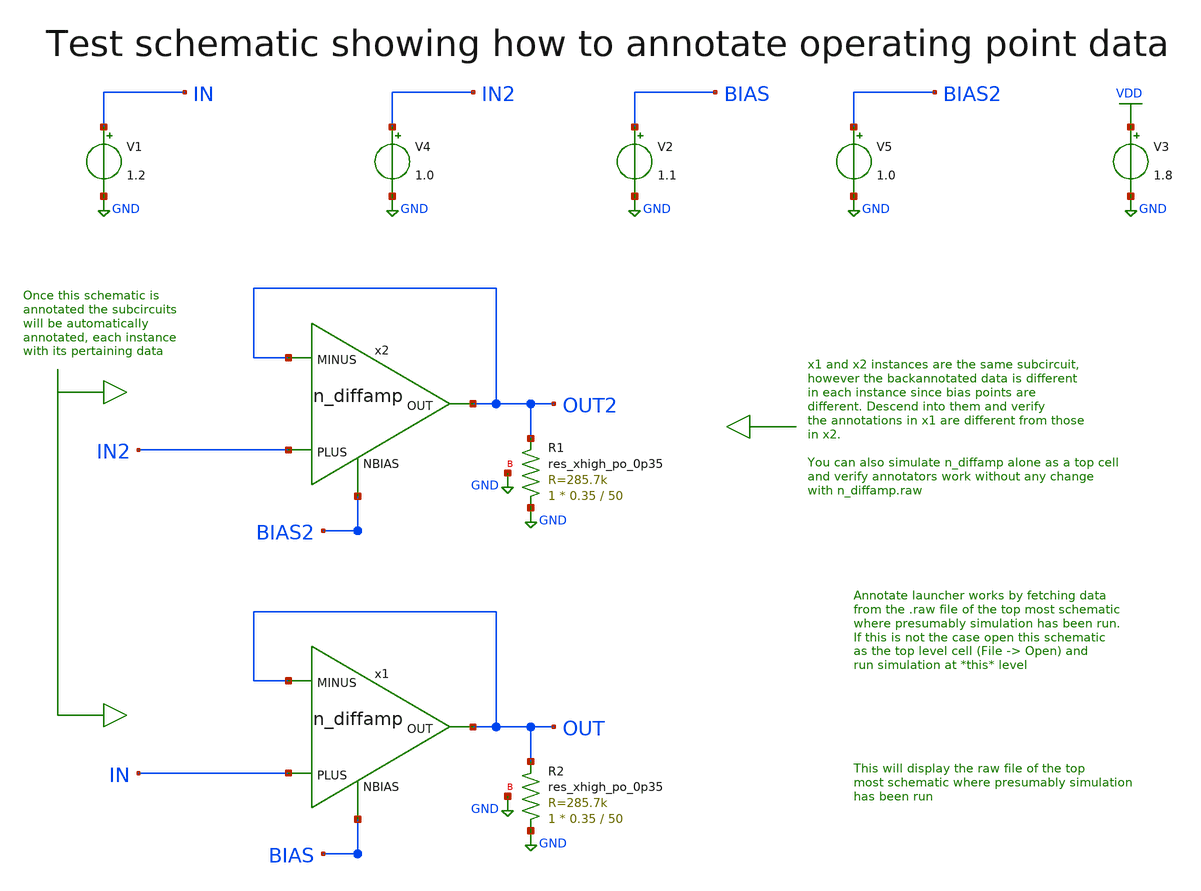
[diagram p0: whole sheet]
** sch_path: sky130_tests/test_analog.sch
* Copyright 2021 Stefan Frederik Schippers
* Licensed under the Apache License, Version 2.0 (the "License");
* you may not use this file except in compliance with the License.
* You may obtain a copy of the License at
* https://www.apache.org/licenses/LICENSE-2.0
* Unless required by applicable law or agreed to in writing, software
* distributed under the License is distributed on an "AS IS" BASIS,
* WITHOUT WARRANTIES OR CONDITIONS OF ANY KIND, either express or implied.
* See the License for the specific language governing permissions and
* limitations under the License.
**.subckt test_analog
x1 OUT OUT IN BIAS n_diffamp
x2 OUT2 OUT2 IN2 BIAS2 n_diffamp
V1 IN GND 1.2
V2 BIAS GND 1.1
V3 VDD GND 1.8
V4 IN2 GND 1.0
V5 BIAS2 GND 1.0
XR1 GND OUT2 GND sky130_fd_pr__res_xhigh_po_0p35 L=50 mult=1 m=1
XR2 GND OUT GND sky130_fd_pr__res_xhigh_po_0p35 L=50 mult=1 m=1
**** begin user architecture code

** opencircuitdesign pdks install
.lib $::SKYWATER_MODELS/sky130.lib.spice tt


**** end user architecture code
**.ends

* expanding   symbol:  sky130_tests/n_diffamp.sym # of pins=4
** sym_path: sky130_tests/n_diffamp.sym
** sch_path: sky130_tests/n_diffamp.sch
.subckt n_diffamp OUT MINUS PLUS NBIAS
*.ipin PLUS
*.ipin MINUS
*.opin OUT
*.ipin NBIAS
XM1 net1 PLUS S GND sky130_fd_pr__nfet_01v8_lvt L=0.3 W=2 nf=1 ad='int((nf+1)/2) * W/nf * 0.29' as='int((nf+2)/2) * W/nf * 0.29'
+ pd='2*int((nf+1)/2) * (W/nf + 0.29)' ps='2*int((nf+2)/2) * (W/nf + 0.29)' nrd='0.29 / W' nrs='0.29 / W'
+ sa=0 sb=0 sd=0 mult=1 m=1
XM2 OUT MINUS S GND sky130_fd_pr__nfet_01v8_lvt L=0.3 W=2 nf=1 ad='int((nf+1)/2) * W/nf * 0.29' as='int((nf+2)/2) * W/nf * 0.29'
+ pd='2*int((nf+1)/2) * (W/nf + 0.29)' ps='2*int((nf+2)/2) * (W/nf + 0.29)' nrd='0.29 / W' nrs='0.29 / W'
+ sa=0 sb=0 sd=0 mult=1 m=1
XM3 OUT net1 VDD VDD sky130_fd_pr__pfet_01v8_lvt L=0.8 W=4 nf=1 ad='int((nf+1)/2) * W/nf * 0.29' as='int((nf+2)/2) * W/nf * 0.29'
+ pd='2*int((nf+1)/2) * (W/nf + 0.29)' ps='2*int((nf+2)/2) * (W/nf + 0.29)' nrd='0.29 / W' nrs='0.29 / W'
+ sa=0 sb=0 sd=0 mult=1 m=1
XM4 net1 net1 VDD VDD sky130_fd_pr__pfet_01v8_lvt L=0.8 W=4 nf=1 ad='int((nf+1)/2) * W/nf * 0.29' as='int((nf+2)/2) * W/nf * 0.29'
+ pd='2*int((nf+1)/2) * (W/nf + 0.29)' ps='2*int((nf+2)/2) * (W/nf + 0.29)' nrd='0.29 / W' nrs='0.29 / W'
+ sa=0 sb=0 sd=0 mult=1 m=1
XM5 net2 NBIAS GND GND sky130_fd_pr__nfet_01v8 L=2 W=0.7 nf=1 ad='int((nf+1)/2) * W/nf * 0.29' as='int((nf+2)/2) * W/nf * 0.29'
+ pd='2*int((nf+1)/2) * (W/nf + 0.29)' ps='2*int((nf+2)/2) * (W/nf + 0.29)' nrd='0.29 / W' nrs='0.29 / W'
+ sa=0 sb=0 sd=0 mult=1 m=1
XR1 GND S GND sky130_fd_pr__res_xhigh_po_0p35 L=50 mult=1 m=1
V5 S net2 0
.save i(v5)
.ends

.GLOBAL GND
.GLOBAL VDD
**** begin user architecture code



.options savecurrents
.control
save all
save @m.x1.xm1.msky130_fd_pr__nfet_01v8_lvt[gm]
save @m.x1.xm2.msky130_fd_pr__nfet_01v8_lvt[gm]
save @m.x1.xm3.msky130_fd_pr__pfet_01v8_lvt[gm]
save @m.x1.xm4.msky130_fd_pr__pfet_01v8_lvt[gm]
save @m.x1.xm5.msky130_fd_pr__nfet_01v8[gm]
save @m.x2.xm1.msky130_fd_pr__nfet_01v8_lvt[gm]
save @m.x2.xm2.msky130_fd_pr__nfet_01v8_lvt[gm]
save @m.x2.xm3.msky130_fd_pr__pfet_01v8_lvt[gm]
save @m.x2.xm4.msky130_fd_pr__pfet_01v8_lvt[gm]
save @m.x2.xm5.msky130_fd_pr__nfet_01v8[gm]
op
write test_analog.raw
.endc


**** end user architecture code
.end
